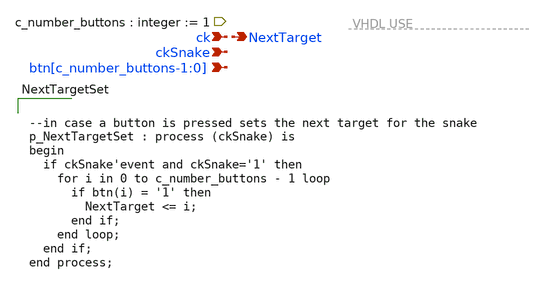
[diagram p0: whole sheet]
** sch_path: xschem/NextTargetSet.sch
**.subckt NextTargetSet ck ckSnake btn[c_number_buttons-1:0] NextTarget
*.ipin ck
*.ipin ckSnake
*.ipin btn[c_number_buttons-1:0]
*.opin NextTarget
**** begin user architecture code


--in case a button is pressed sets the next target for the snake
p_NextTargetSet : process (ckSnake) is
begin
  if ckSnake'event and ckSnake='1' then
    for i in 0 to c_number_buttons - 1 loop
      if btn(i) = '1' then
        NextTarget <= i;
      end if;
    end loop;
  end if;
end process;


**** end user architecture code
**.ends
.end
